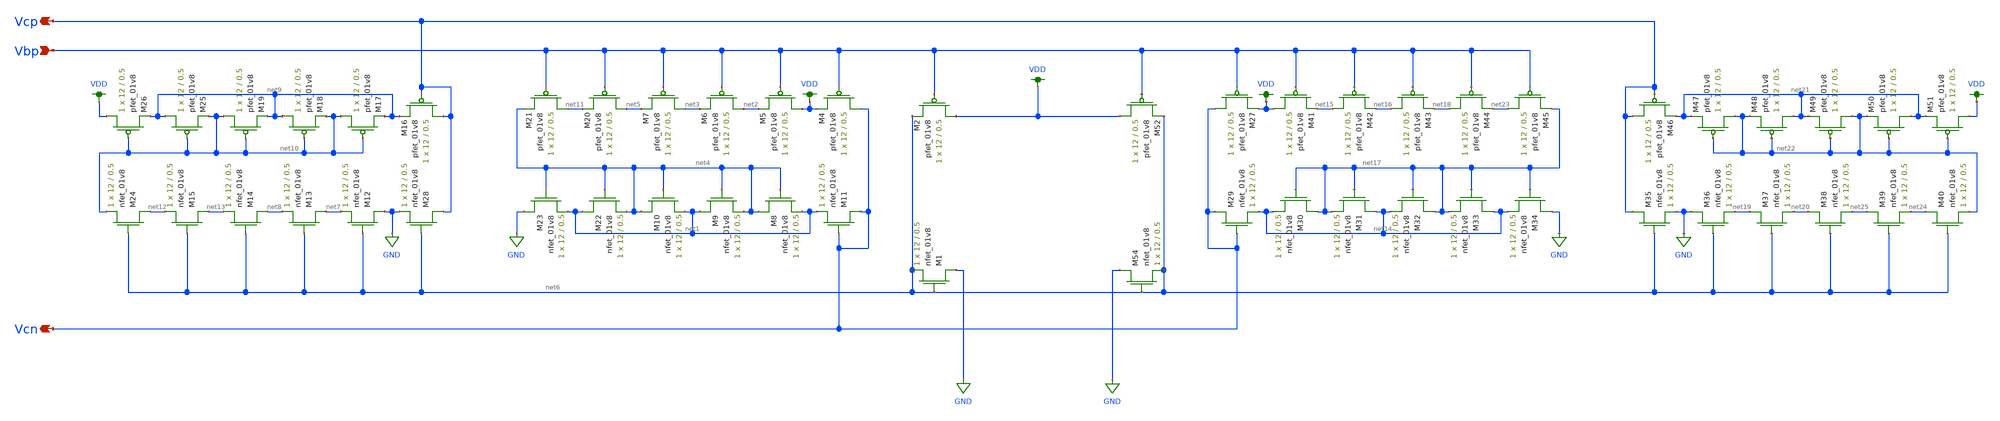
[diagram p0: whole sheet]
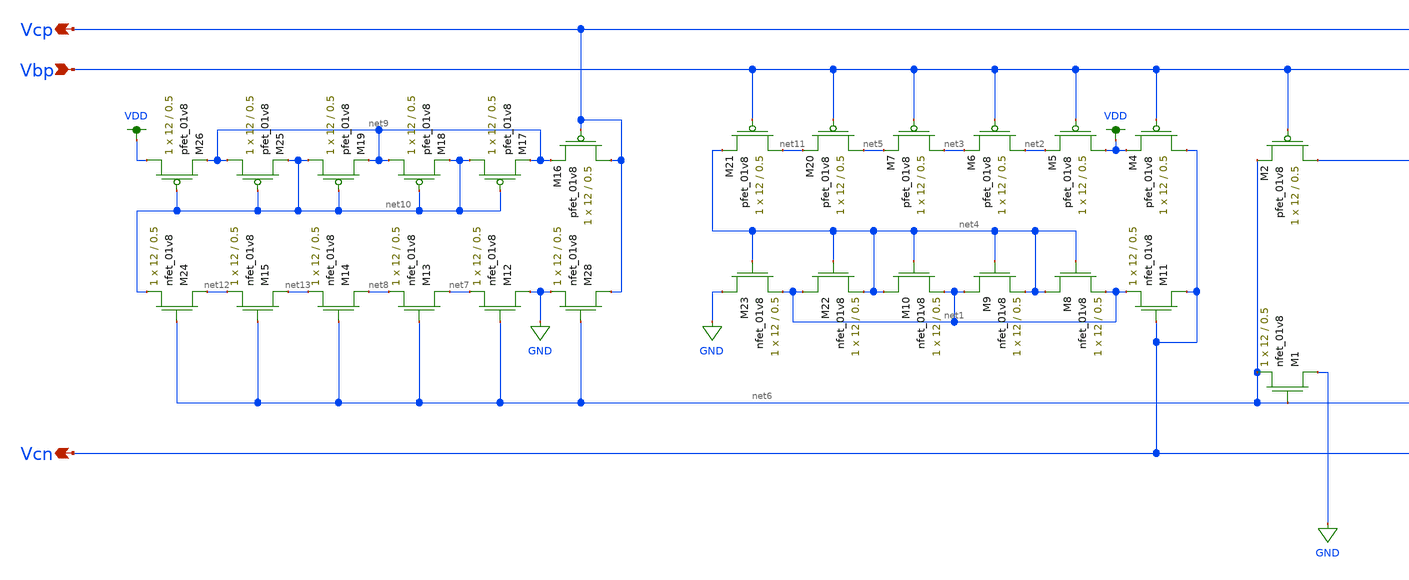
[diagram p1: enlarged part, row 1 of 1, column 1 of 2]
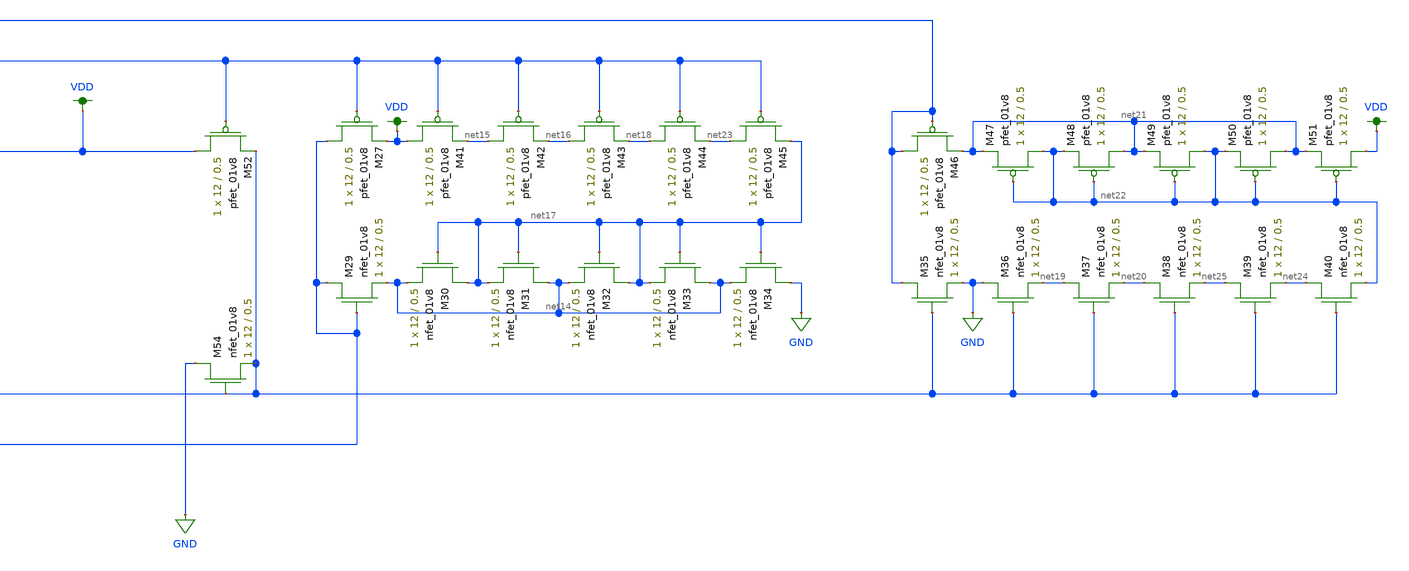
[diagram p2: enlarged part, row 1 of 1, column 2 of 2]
** sch_path: modules/bias_current_generator_lds.sch
**.subckt bias_current_generator_lds Vcn Vcp Vbp
*.opin Vcn
*.opin Vcp
*.ipin Vbp
XM4 Vcn Vbp VDD VDD sky130_fd_pr__pfet_01v8 L=0.5 W=12 nf=1 ad='int((nf+1)/2) * W/nf * 0.29' as='int((nf+2)/2) * W/nf * 0.29'
+ pd='2*int((nf+1)/2) * (W/nf + 0.29)' ps='2*int((nf+2)/2) * (W/nf + 0.29)' nrd='0.29 / W' nrs='0.29 / W'
+ sa=0 sb=0 sd=0 mult=1 m=1
XM11 Vcn Vcn net1 GND sky130_fd_pr__nfet_01v8 L=0.5 W=12 nf=1 ad='int((nf+1)/2) * W/nf * 0.29' as='int((nf+2)/2) * W/nf * 0.29'
+ pd='2*int((nf+1)/2) * (W/nf + 0.29)' ps='2*int((nf+2)/2) * (W/nf + 0.29)' nrd='0.29 / W' nrs='0.29 / W'
+ sa=0 sb=0 sd=0 mult=1 m=1
XM8 net4 net4 net1 GND sky130_fd_pr__nfet_01v8 L=0.5 W=12 nf=1 ad='int((nf+1)/2) * W/nf * 0.29' as='int((nf+2)/2) * W/nf * 0.29'
+ pd='2*int((nf+1)/2) * (W/nf + 0.29)' ps='2*int((nf+2)/2) * (W/nf + 0.29)' nrd='0.29 / W' nrs='0.29 / W'
+ sa=0 sb=0 sd=0 mult=1 m=1
XM9 net1 net4 net4 GND sky130_fd_pr__nfet_01v8 L=0.5 W=12 nf=1 ad='int((nf+1)/2) * W/nf * 0.29' as='int((nf+2)/2) * W/nf * 0.29'
+ pd='2*int((nf+1)/2) * (W/nf + 0.29)' ps='2*int((nf+2)/2) * (W/nf + 0.29)' nrd='0.29 / W' nrs='0.29 / W'
+ sa=0 sb=0 sd=0 mult=1 m=1
XM10 net4 net4 net1 GND sky130_fd_pr__nfet_01v8 L=0.5 W=12 nf=1 ad='int((nf+1)/2) * W/nf * 0.29' as='int((nf+2)/2) * W/nf * 0.29'
+ pd='2*int((nf+1)/2) * (W/nf + 0.29)' ps='2*int((nf+2)/2) * (W/nf + 0.29)' nrd='0.29 / W' nrs='0.29 / W'
+ sa=0 sb=0 sd=0 mult=1 m=1
XM22 net1 net4 net4 GND sky130_fd_pr__nfet_01v8 L=0.5 W=12 nf=1 ad='int((nf+1)/2) * W/nf * 0.29' as='int((nf+2)/2) * W/nf * 0.29'
+ pd='2*int((nf+1)/2) * (W/nf + 0.29)' ps='2*int((nf+2)/2) * (W/nf + 0.29)' nrd='0.29 / W' nrs='0.29 / W'
+ sa=0 sb=0 sd=0 mult=1 m=1
XM23 GND net4 net1 GND sky130_fd_pr__nfet_01v8 L=0.5 W=12 nf=1 ad='int((nf+1)/2) * W/nf * 0.29' as='int((nf+2)/2) * W/nf * 0.29'
+ pd='2*int((nf+1)/2) * (W/nf + 0.29)' ps='2*int((nf+2)/2) * (W/nf + 0.29)' nrd='0.29 / W' nrs='0.29 / W'
+ sa=0 sb=0 sd=0 mult=1 m=1
XM28 Vcp net6 GND GND sky130_fd_pr__nfet_01v8 L=0.5 W=12 nf=1 ad='int((nf+1)/2) * W/nf * 0.29' as='int((nf+2)/2) * W/nf * 0.29'
+ pd='2*int((nf+1)/2) * (W/nf + 0.29)' ps='2*int((nf+2)/2) * (W/nf + 0.29)' nrd='0.29 / W' nrs='0.29 / W'
+ sa=0 sb=0 sd=0 mult=1 m=1
XM12 GND net6 net7 GND sky130_fd_pr__nfet_01v8 L=0.5 W=12 nf=1 ad='int((nf+1)/2) * W/nf * 0.29' as='int((nf+2)/2) * W/nf * 0.29'
+ pd='2*int((nf+1)/2) * (W/nf + 0.29)' ps='2*int((nf+2)/2) * (W/nf + 0.29)' nrd='0.29 / W' nrs='0.29 / W'
+ sa=0 sb=0 sd=0 mult=1 m=1
XM13 net7 net6 net8 GND sky130_fd_pr__nfet_01v8 L=0.5 W=12 nf=1 ad='int((nf+1)/2) * W/nf * 0.29' as='int((nf+2)/2) * W/nf * 0.29'
+ pd='2*int((nf+1)/2) * (W/nf + 0.29)' ps='2*int((nf+2)/2) * (W/nf + 0.29)' nrd='0.29 / W' nrs='0.29 / W'
+ sa=0 sb=0 sd=0 mult=1 m=1
XM14 net8 net6 net13 GND sky130_fd_pr__nfet_01v8 L=0.5 W=12 nf=1 ad='int((nf+1)/2) * W/nf * 0.29' as='int((nf+2)/2) * W/nf * 0.29'
+ pd='2*int((nf+1)/2) * (W/nf + 0.29)' ps='2*int((nf+2)/2) * (W/nf + 0.29)' nrd='0.29 / W' nrs='0.29 / W'
+ sa=0 sb=0 sd=0 mult=1 m=1
XM15 net13 net6 net12 GND sky130_fd_pr__nfet_01v8 L=0.5 W=12 nf=1 ad='int((nf+1)/2) * W/nf * 0.29' as='int((nf+2)/2) * W/nf * 0.29'
+ pd='2*int((nf+1)/2) * (W/nf + 0.29)' ps='2*int((nf+2)/2) * (W/nf + 0.29)' nrd='0.29 / W' nrs='0.29 / W'
+ sa=0 sb=0 sd=0 mult=1 m=1
XM24 net12 net6 net10 GND sky130_fd_pr__nfet_01v8 L=0.5 W=12 nf=1 ad='int((nf+1)/2) * W/nf * 0.29' as='int((nf+2)/2) * W/nf * 0.29'
+ pd='2*int((nf+1)/2) * (W/nf + 0.29)' ps='2*int((nf+2)/2) * (W/nf + 0.29)' nrd='0.29 / W' nrs='0.29 / W'
+ sa=0 sb=0 sd=0 mult=1 m=1
XM5 VDD Vbp net2 VDD sky130_fd_pr__pfet_01v8 L=0.5 W=12 nf=1 ad='int((nf+1)/2) * W/nf * 0.29' as='int((nf+2)/2) * W/nf * 0.29'
+ pd='2*int((nf+1)/2) * (W/nf + 0.29)' ps='2*int((nf+2)/2) * (W/nf + 0.29)' nrd='0.29 / W' nrs='0.29 / W'
+ sa=0 sb=0 sd=0 mult=1 m=1
XM6 net2 Vbp net3 VDD sky130_fd_pr__pfet_01v8 L=0.5 W=12 nf=1 ad='int((nf+1)/2) * W/nf * 0.29' as='int((nf+2)/2) * W/nf * 0.29'
+ pd='2*int((nf+1)/2) * (W/nf + 0.29)' ps='2*int((nf+2)/2) * (W/nf + 0.29)' nrd='0.29 / W' nrs='0.29 / W'
+ sa=0 sb=0 sd=0 mult=1 m=1
XM7 net3 Vbp net5 VDD sky130_fd_pr__pfet_01v8 L=0.5 W=12 nf=1 ad='int((nf+1)/2) * W/nf * 0.29' as='int((nf+2)/2) * W/nf * 0.29'
+ pd='2*int((nf+1)/2) * (W/nf + 0.29)' ps='2*int((nf+2)/2) * (W/nf + 0.29)' nrd='0.29 / W' nrs='0.29 / W'
+ sa=0 sb=0 sd=0 mult=1 m=1
XM20 net5 Vbp net11 VDD sky130_fd_pr__pfet_01v8 L=0.5 W=12 nf=1 ad='int((nf+1)/2) * W/nf * 0.29' as='int((nf+2)/2) * W/nf * 0.29'
+ pd='2*int((nf+1)/2) * (W/nf + 0.29)' ps='2*int((nf+2)/2) * (W/nf + 0.29)' nrd='0.29 / W' nrs='0.29 / W'
+ sa=0 sb=0 sd=0 mult=1 m=1
XM21 net11 Vbp net4 VDD sky130_fd_pr__pfet_01v8 L=0.5 W=12 nf=1 ad='int((nf+1)/2) * W/nf * 0.29' as='int((nf+2)/2) * W/nf * 0.29'
+ pd='2*int((nf+1)/2) * (W/nf + 0.29)' ps='2*int((nf+2)/2) * (W/nf + 0.29)' nrd='0.29 / W' nrs='0.29 / W'
+ sa=0 sb=0 sd=0 mult=1 m=1
XM16 Vcp Vcp net9 VDD sky130_fd_pr__pfet_01v8 L=0.5 W=12 nf=1 ad='int((nf+1)/2) * W/nf * 0.29' as='int((nf+2)/2) * W/nf * 0.29'
+ pd='2*int((nf+1)/2) * (W/nf + 0.29)' ps='2*int((nf+2)/2) * (W/nf + 0.29)' nrd='0.29 / W' nrs='0.29 / W'
+ sa=0 sb=0 sd=0 mult=1 m=1
XM17 net10 net10 net9 VDD sky130_fd_pr__pfet_01v8 L=0.5 W=12 nf=1 ad='int((nf+1)/2) * W/nf * 0.29' as='int((nf+2)/2) * W/nf * 0.29'
+ pd='2*int((nf+1)/2) * (W/nf + 0.29)' ps='2*int((nf+2)/2) * (W/nf + 0.29)' nrd='0.29 / W' nrs='0.29 / W'
+ sa=0 sb=0 sd=0 mult=1 m=1
XM18 net9 net10 net10 VDD sky130_fd_pr__pfet_01v8 L=0.5 W=12 nf=1 ad='int((nf+1)/2) * W/nf * 0.29' as='int((nf+2)/2) * W/nf * 0.29'
+ pd='2*int((nf+1)/2) * (W/nf + 0.29)' ps='2*int((nf+2)/2) * (W/nf + 0.29)' nrd='0.29 / W' nrs='0.29 / W'
+ sa=0 sb=0 sd=0 mult=1 m=1
XM19 net10 net10 net9 VDD sky130_fd_pr__pfet_01v8 L=0.5 W=12 nf=1 ad='int((nf+1)/2) * W/nf * 0.29' as='int((nf+2)/2) * W/nf * 0.29'
+ pd='2*int((nf+1)/2) * (W/nf + 0.29)' ps='2*int((nf+2)/2) * (W/nf + 0.29)' nrd='0.29 / W' nrs='0.29 / W'
+ sa=0 sb=0 sd=0 mult=1 m=1
XM25 net9 net10 net10 VDD sky130_fd_pr__pfet_01v8 L=0.5 W=12 nf=1 ad='int((nf+1)/2) * W/nf * 0.29' as='int((nf+2)/2) * W/nf * 0.29'
+ pd='2*int((nf+1)/2) * (W/nf + 0.29)' ps='2*int((nf+2)/2) * (W/nf + 0.29)' nrd='0.29 / W' nrs='0.29 / W'
+ sa=0 sb=0 sd=0 mult=1 m=1
XM26 VDD net10 net9 VDD sky130_fd_pr__pfet_01v8 L=0.5 W=12 nf=1 ad='int((nf+1)/2) * W/nf * 0.29' as='int((nf+2)/2) * W/nf * 0.29'
+ pd='2*int((nf+1)/2) * (W/nf + 0.29)' ps='2*int((nf+2)/2) * (W/nf + 0.29)' nrd='0.29 / W' nrs='0.29 / W'
+ sa=0 sb=0 sd=0 mult=1 m=1
XM2 VDD Vbp net6 VDD sky130_fd_pr__pfet_01v8 L=0.5 W=12 nf=1 ad='int((nf+1)/2) * W/nf * 0.29' as='int((nf+2)/2) * W/nf * 0.29'
+ pd='2*int((nf+1)/2) * (W/nf + 0.29)' ps='2*int((nf+2)/2) * (W/nf + 0.29)' nrd='0.29 / W' nrs='0.29 / W'
+ sa=0 sb=0 sd=0 mult=1 m=1
XM1 GND net6 net6 GND sky130_fd_pr__nfet_01v8 L=0.5 W=12 nf=1 ad='int((nf+1)/2) * W/nf * 0.29' as='int((nf+2)/2) * W/nf * 0.29'
+ pd='2*int((nf+1)/2) * (W/nf + 0.29)' ps='2*int((nf+2)/2) * (W/nf + 0.29)' nrd='0.29 / W' nrs='0.29 / W'
+ sa=0 sb=0 sd=0 mult=1 m=1
XM27 Vcn Vbp VDD VDD sky130_fd_pr__pfet_01v8 L=0.5 W=12 nf=1 ad='int((nf+1)/2) * W/nf * 0.29' as='int((nf+2)/2) * W/nf * 0.29'
+ pd='2*int((nf+1)/2) * (W/nf + 0.29)' ps='2*int((nf+2)/2) * (W/nf + 0.29)' nrd='0.29 / W' nrs='0.29 / W'
+ sa=0 sb=0 sd=0 mult=1 m=1
XM29 Vcn Vcn net14 GND sky130_fd_pr__nfet_01v8 L=0.5 W=12 nf=1 ad='int((nf+1)/2) * W/nf * 0.29' as='int((nf+2)/2) * W/nf * 0.29'
+ pd='2*int((nf+1)/2) * (W/nf + 0.29)' ps='2*int((nf+2)/2) * (W/nf + 0.29)' nrd='0.29 / W' nrs='0.29 / W'
+ sa=0 sb=0 sd=0 mult=1 m=1
XM30 net17 net17 net14 GND sky130_fd_pr__nfet_01v8 L=0.5 W=12 nf=1 ad='int((nf+1)/2) * W/nf * 0.29' as='int((nf+2)/2) * W/nf * 0.29'
+ pd='2*int((nf+1)/2) * (W/nf + 0.29)' ps='2*int((nf+2)/2) * (W/nf + 0.29)' nrd='0.29 / W' nrs='0.29 / W'
+ sa=0 sb=0 sd=0 mult=1 m=1
XM31 net14 net17 net17 GND sky130_fd_pr__nfet_01v8 L=0.5 W=12 nf=1 ad='int((nf+1)/2) * W/nf * 0.29' as='int((nf+2)/2) * W/nf * 0.29'
+ pd='2*int((nf+1)/2) * (W/nf + 0.29)' ps='2*int((nf+2)/2) * (W/nf + 0.29)' nrd='0.29 / W' nrs='0.29 / W'
+ sa=0 sb=0 sd=0 mult=1 m=1
XM32 net17 net17 net14 GND sky130_fd_pr__nfet_01v8 L=0.5 W=12 nf=1 ad='int((nf+1)/2) * W/nf * 0.29' as='int((nf+2)/2) * W/nf * 0.29'
+ pd='2*int((nf+1)/2) * (W/nf + 0.29)' ps='2*int((nf+2)/2) * (W/nf + 0.29)' nrd='0.29 / W' nrs='0.29 / W'
+ sa=0 sb=0 sd=0 mult=1 m=1
XM33 net14 net17 net17 GND sky130_fd_pr__nfet_01v8 L=0.5 W=12 nf=1 ad='int((nf+1)/2) * W/nf * 0.29' as='int((nf+2)/2) * W/nf * 0.29'
+ pd='2*int((nf+1)/2) * (W/nf + 0.29)' ps='2*int((nf+2)/2) * (W/nf + 0.29)' nrd='0.29 / W' nrs='0.29 / W'
+ sa=0 sb=0 sd=0 mult=1 m=1
XM34 GND net17 net14 GND sky130_fd_pr__nfet_01v8 L=0.5 W=12 nf=1 ad='int((nf+1)/2) * W/nf * 0.29' as='int((nf+2)/2) * W/nf * 0.29'
+ pd='2*int((nf+1)/2) * (W/nf + 0.29)' ps='2*int((nf+2)/2) * (W/nf + 0.29)' nrd='0.29 / W' nrs='0.29 / W'
+ sa=0 sb=0 sd=0 mult=1 m=1
XM35 Vcp net6 GND GND sky130_fd_pr__nfet_01v8 L=0.5 W=12 nf=1 ad='int((nf+1)/2) * W/nf * 0.29' as='int((nf+2)/2) * W/nf * 0.29'
+ pd='2*int((nf+1)/2) * (W/nf + 0.29)' ps='2*int((nf+2)/2) * (W/nf + 0.29)' nrd='0.29 / W' nrs='0.29 / W'
+ sa=0 sb=0 sd=0 mult=1 m=1
XM36 GND net6 net19 GND sky130_fd_pr__nfet_01v8 L=0.5 W=12 nf=1 ad='int((nf+1)/2) * W/nf * 0.29' as='int((nf+2)/2) * W/nf * 0.29'
+ pd='2*int((nf+1)/2) * (W/nf + 0.29)' ps='2*int((nf+2)/2) * (W/nf + 0.29)' nrd='0.29 / W' nrs='0.29 / W'
+ sa=0 sb=0 sd=0 mult=1 m=1
XM37 net19 net6 net20 GND sky130_fd_pr__nfet_01v8 L=0.5 W=12 nf=1 ad='int((nf+1)/2) * W/nf * 0.29' as='int((nf+2)/2) * W/nf * 0.29'
+ pd='2*int((nf+1)/2) * (W/nf + 0.29)' ps='2*int((nf+2)/2) * (W/nf + 0.29)' nrd='0.29 / W' nrs='0.29 / W'
+ sa=0 sb=0 sd=0 mult=1 m=1
XM38 net20 net6 net25 GND sky130_fd_pr__nfet_01v8 L=0.5 W=12 nf=1 ad='int((nf+1)/2) * W/nf * 0.29' as='int((nf+2)/2) * W/nf * 0.29'
+ pd='2*int((nf+1)/2) * (W/nf + 0.29)' ps='2*int((nf+2)/2) * (W/nf + 0.29)' nrd='0.29 / W' nrs='0.29 / W'
+ sa=0 sb=0 sd=0 mult=1 m=1
XM39 net25 net6 net24 GND sky130_fd_pr__nfet_01v8 L=0.5 W=12 nf=1 ad='int((nf+1)/2) * W/nf * 0.29' as='int((nf+2)/2) * W/nf * 0.29'
+ pd='2*int((nf+1)/2) * (W/nf + 0.29)' ps='2*int((nf+2)/2) * (W/nf + 0.29)' nrd='0.29 / W' nrs='0.29 / W'
+ sa=0 sb=0 sd=0 mult=1 m=1
XM40 net24 net6 net22 GND sky130_fd_pr__nfet_01v8 L=0.5 W=12 nf=1 ad='int((nf+1)/2) * W/nf * 0.29' as='int((nf+2)/2) * W/nf * 0.29'
+ pd='2*int((nf+1)/2) * (W/nf + 0.29)' ps='2*int((nf+2)/2) * (W/nf + 0.29)' nrd='0.29 / W' nrs='0.29 / W'
+ sa=0 sb=0 sd=0 mult=1 m=1
XM41 VDD Vbp net15 VDD sky130_fd_pr__pfet_01v8 L=0.5 W=12 nf=1 ad='int((nf+1)/2) * W/nf * 0.29' as='int((nf+2)/2) * W/nf * 0.29'
+ pd='2*int((nf+1)/2) * (W/nf + 0.29)' ps='2*int((nf+2)/2) * (W/nf + 0.29)' nrd='0.29 / W' nrs='0.29 / W'
+ sa=0 sb=0 sd=0 mult=1 m=1
XM42 net15 Vbp net16 VDD sky130_fd_pr__pfet_01v8 L=0.5 W=12 nf=1 ad='int((nf+1)/2) * W/nf * 0.29' as='int((nf+2)/2) * W/nf * 0.29'
+ pd='2*int((nf+1)/2) * (W/nf + 0.29)' ps='2*int((nf+2)/2) * (W/nf + 0.29)' nrd='0.29 / W' nrs='0.29 / W'
+ sa=0 sb=0 sd=0 mult=1 m=1
XM43 net16 Vbp net18 VDD sky130_fd_pr__pfet_01v8 L=0.5 W=12 nf=1 ad='int((nf+1)/2) * W/nf * 0.29' as='int((nf+2)/2) * W/nf * 0.29'
+ pd='2*int((nf+1)/2) * (W/nf + 0.29)' ps='2*int((nf+2)/2) * (W/nf + 0.29)' nrd='0.29 / W' nrs='0.29 / W'
+ sa=0 sb=0 sd=0 mult=1 m=1
XM44 net18 Vbp net23 VDD sky130_fd_pr__pfet_01v8 L=0.5 W=12 nf=1 ad='int((nf+1)/2) * W/nf * 0.29' as='int((nf+2)/2) * W/nf * 0.29'
+ pd='2*int((nf+1)/2) * (W/nf + 0.29)' ps='2*int((nf+2)/2) * (W/nf + 0.29)' nrd='0.29 / W' nrs='0.29 / W'
+ sa=0 sb=0 sd=0 mult=1 m=1
XM45 net23 Vbp net17 VDD sky130_fd_pr__pfet_01v8 L=0.5 W=12 nf=1 ad='int((nf+1)/2) * W/nf * 0.29' as='int((nf+2)/2) * W/nf * 0.29'
+ pd='2*int((nf+1)/2) * (W/nf + 0.29)' ps='2*int((nf+2)/2) * (W/nf + 0.29)' nrd='0.29 / W' nrs='0.29 / W'
+ sa=0 sb=0 sd=0 mult=1 m=1
XM46 Vcp Vcp net21 VDD sky130_fd_pr__pfet_01v8 L=0.5 W=12 nf=1 ad='int((nf+1)/2) * W/nf * 0.29' as='int((nf+2)/2) * W/nf * 0.29'
+ pd='2*int((nf+1)/2) * (W/nf + 0.29)' ps='2*int((nf+2)/2) * (W/nf + 0.29)' nrd='0.29 / W' nrs='0.29 / W'
+ sa=0 sb=0 sd=0 mult=1 m=1
XM47 net22 net22 net21 VDD sky130_fd_pr__pfet_01v8 L=0.5 W=12 nf=1 ad='int((nf+1)/2) * W/nf * 0.29' as='int((nf+2)/2) * W/nf * 0.29'
+ pd='2*int((nf+1)/2) * (W/nf + 0.29)' ps='2*int((nf+2)/2) * (W/nf + 0.29)' nrd='0.29 / W' nrs='0.29 / W'
+ sa=0 sb=0 sd=0 mult=1 m=1
XM48 net21 net22 net22 VDD sky130_fd_pr__pfet_01v8 L=0.5 W=12 nf=1 ad='int((nf+1)/2) * W/nf * 0.29' as='int((nf+2)/2) * W/nf * 0.29'
+ pd='2*int((nf+1)/2) * (W/nf + 0.29)' ps='2*int((nf+2)/2) * (W/nf + 0.29)' nrd='0.29 / W' nrs='0.29 / W'
+ sa=0 sb=0 sd=0 mult=1 m=1
XM49 net22 net22 net21 VDD sky130_fd_pr__pfet_01v8 L=0.5 W=12 nf=1 ad='int((nf+1)/2) * W/nf * 0.29' as='int((nf+2)/2) * W/nf * 0.29'
+ pd='2*int((nf+1)/2) * (W/nf + 0.29)' ps='2*int((nf+2)/2) * (W/nf + 0.29)' nrd='0.29 / W' nrs='0.29 / W'
+ sa=0 sb=0 sd=0 mult=1 m=1
XM50 net21 net22 net22 VDD sky130_fd_pr__pfet_01v8 L=0.5 W=12 nf=1 ad='int((nf+1)/2) * W/nf * 0.29' as='int((nf+2)/2) * W/nf * 0.29'
+ pd='2*int((nf+1)/2) * (W/nf + 0.29)' ps='2*int((nf+2)/2) * (W/nf + 0.29)' nrd='0.29 / W' nrs='0.29 / W'
+ sa=0 sb=0 sd=0 mult=1 m=1
XM51 VDD net22 net21 VDD sky130_fd_pr__pfet_01v8 L=0.5 W=12 nf=1 ad='int((nf+1)/2) * W/nf * 0.29' as='int((nf+2)/2) * W/nf * 0.29'
+ pd='2*int((nf+1)/2) * (W/nf + 0.29)' ps='2*int((nf+2)/2) * (W/nf + 0.29)' nrd='0.29 / W' nrs='0.29 / W'
+ sa=0 sb=0 sd=0 mult=1 m=1
XM52 VDD Vbp net6 VDD sky130_fd_pr__pfet_01v8 L=0.5 W=12 nf=1 ad='int((nf+1)/2) * W/nf * 0.29' as='int((nf+2)/2) * W/nf * 0.29'
+ pd='2*int((nf+1)/2) * (W/nf + 0.29)' ps='2*int((nf+2)/2) * (W/nf + 0.29)' nrd='0.29 / W' nrs='0.29 / W'
+ sa=0 sb=0 sd=0 mult=1 m=1
XM54 GND net6 net6 GND sky130_fd_pr__nfet_01v8 L=0.5 W=12 nf=1 ad='int((nf+1)/2) * W/nf * 0.29' as='int((nf+2)/2) * W/nf * 0.29'
+ pd='2*int((nf+1)/2) * (W/nf + 0.29)' ps='2*int((nf+2)/2) * (W/nf + 0.29)' nrd='0.29 / W' nrs='0.29 / W'
+ sa=0 sb=0 sd=0 mult=1 m=1
**.ends
.GLOBAL GND
.GLOBAL VDD
.end
